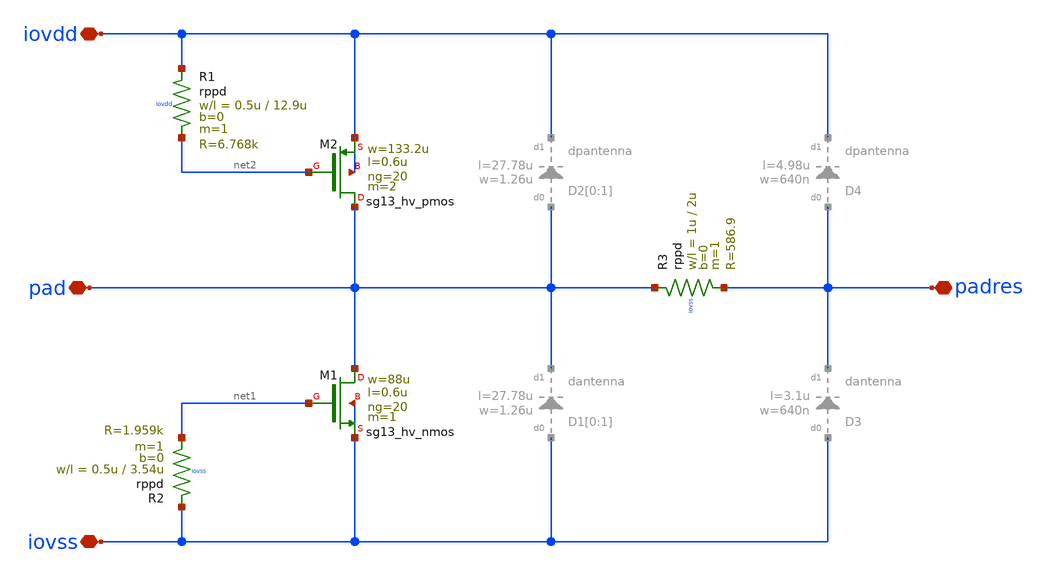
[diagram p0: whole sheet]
** sch_path: xschem/pad_model.sch
**.subckt pad_model pad padres iovdd iovss
*.iopin pad
*.iopin padres
*.iopin iovdd
*.iopin iovss
XM2 pad net2 iovdd iovdd sg13_hv_pmos w=133.2u l=0.6u ng=20 m=2 mm_ok=1
XM1 pad net1 iovss iovss sg13_hv_nmos w=88u l=0.6u ng=20 m=1 mm_ok=1
XR1 iovdd net2 iovdd rppd w=0.5u l=12.9u m=1 b=0 mm_ok=1
XR2 iovss net1 iovss rppd w=0.5u l=3.54u m=1 b=0 mm_ok=1
XR3 pad padres iovss rppd w=1u l=2u m=1 b=0 mm_ok=1
**.ends
.end
